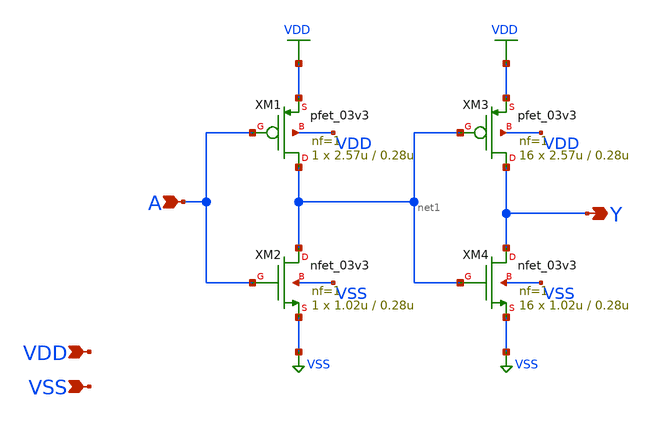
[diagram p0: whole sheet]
** sch_path: xschem/gf180mcu_ocd_sc_rt12t3v3__clkbuf_16.sch
**.subckt gf180mcu_ocd_sc_rt12t3v3__clkbuf_16 A Y VDD VSS
*.ipin A
*.opin Y
*.ipin VDD
*.ipin VSS
XM1 net1 A VDD VDD pfet_03v3 L=0.28u W=2.57u nf=1 ad='int((nf+1)/2) * W/nf * 0.18u' as='int((nf+2)/2) * W/nf * 0.18u'
+ pd='2*int((nf+1)/2) * (W/nf + 0.18u)' ps='2*int((nf+2)/2) * (W/nf + 0.18u)' nrd='0.18u / W' nrs='0.18u / W'
+ sa=0 sb=0 sd=0 m=1
XM2 net1 A VSS VSS nfet_03v3 L=0.28u W=1.02u nf=1 ad='int((nf+1)/2) * W/nf * 0.18u' as='int((nf+2)/2) * W/nf * 0.18u'
+ pd='2*int((nf+1)/2) * (W/nf + 0.18u)' ps='2*int((nf+2)/2) * (W/nf + 0.18u)' nrd='0.18u / W' nrs='0.18u / W'
+ sa=0 sb=0 sd=0 m=1
XM3 Y net1 VDD VDD pfet_03v3 L=0.28u W=2.57u nf=1 ad='int((nf+1)/2) * W/nf * 0.18u' as='int((nf+2)/2) * W/nf * 0.18u'
+ pd='2*int((nf+1)/2) * (W/nf + 0.18u)' ps='2*int((nf+2)/2) * (W/nf + 0.18u)' nrd='0.18u / W' nrs='0.18u / W'
+ sa=0 sb=0 sd=0 m=16
XM4 Y net1 VSS VSS nfet_03v3 L=0.28u W=1.02u nf=1 ad='int((nf+1)/2) * W/nf * 0.18u' as='int((nf+2)/2) * W/nf * 0.18u'
+ pd='2*int((nf+1)/2) * (W/nf + 0.18u)' ps='2*int((nf+2)/2) * (W/nf + 0.18u)' nrd='0.18u / W' nrs='0.18u / W'
+ sa=0 sb=0 sd=0 m=16
**.ends
.GLOBAL VDD
.GLOBAL VSS
.end
